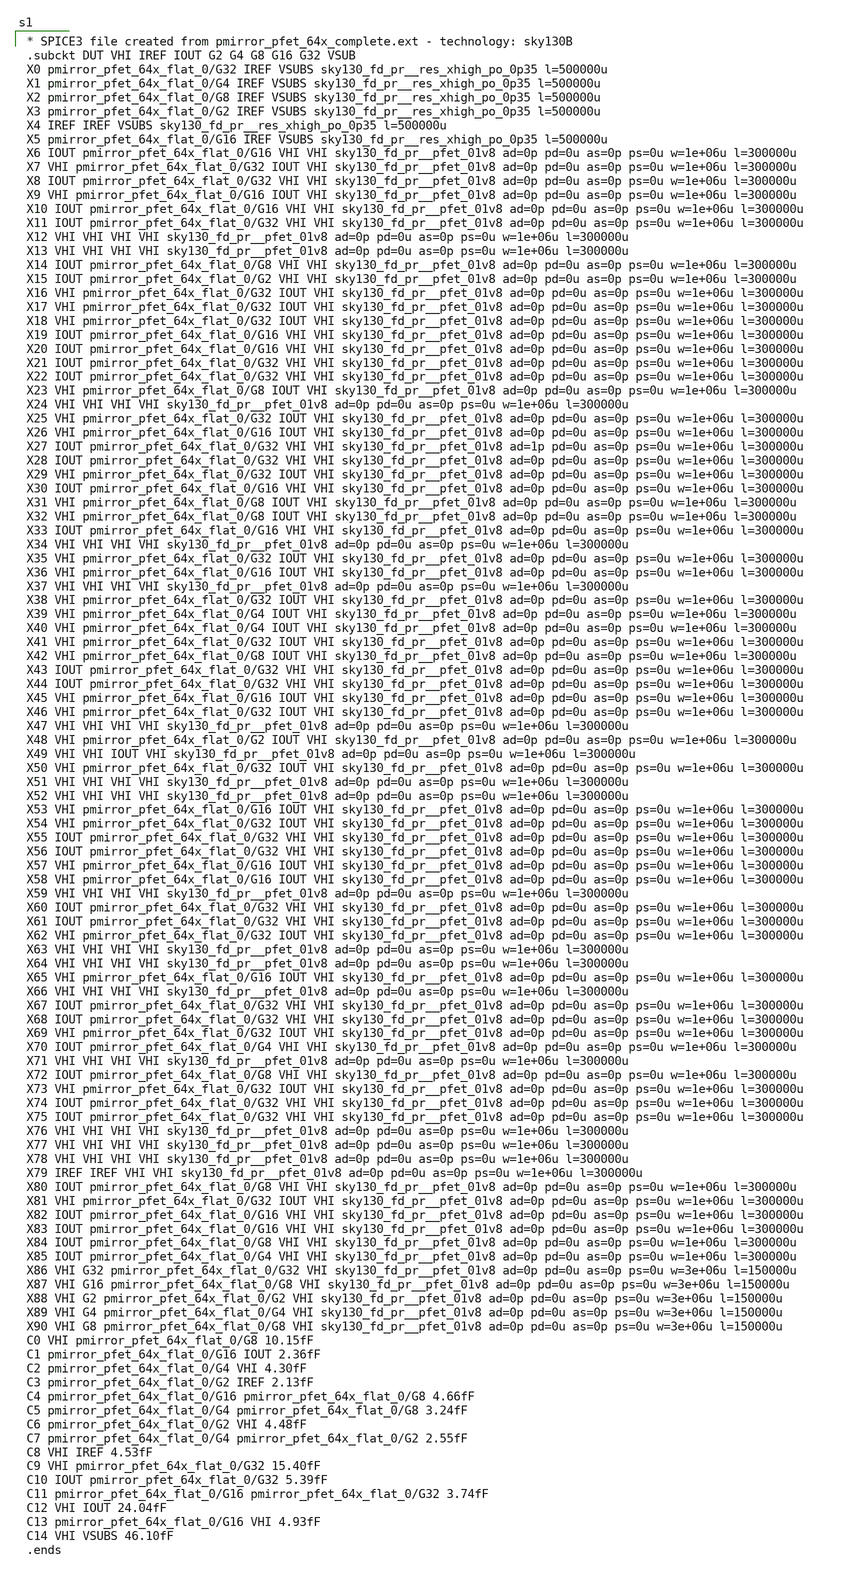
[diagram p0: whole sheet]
** sch_path: xschem/untitled-10.sch
**.subckt untitled-10
**** begin user architecture code

* SPICE3 file created from pmirror_pfet_64x_complete.ext - technology: sky130B
.subckt DUT VHI IREF IOUT G2 G4 G8 G16 G32 VSUB
X0 pmirror_pfet_64x_flat_0/G32 IREF VSUBS sky130_fd_pr__res_xhigh_po_0p35 l=500000u
X1 pmirror_pfet_64x_flat_0/G4 IREF VSUBS sky130_fd_pr__res_xhigh_po_0p35 l=500000u
X2 pmirror_pfet_64x_flat_0/G8 IREF VSUBS sky130_fd_pr__res_xhigh_po_0p35 l=500000u
X3 pmirror_pfet_64x_flat_0/G2 IREF VSUBS sky130_fd_pr__res_xhigh_po_0p35 l=500000u
X4 IREF IREF VSUBS sky130_fd_pr__res_xhigh_po_0p35 l=500000u
X5 pmirror_pfet_64x_flat_0/G16 IREF VSUBS sky130_fd_pr__res_xhigh_po_0p35 l=500000u
X6 IOUT pmirror_pfet_64x_flat_0/G16 VHI VHI sky130_fd_pr__pfet_01v8 ad=0p pd=0u as=0p ps=0u w=1e+06u
+ l=300000u
X7 VHI pmirror_pfet_64x_flat_0/G32 IOUT VHI sky130_fd_pr__pfet_01v8 ad=0p pd=0u as=0p ps=0u w=1e+06u
+ l=300000u
X8 IOUT pmirror_pfet_64x_flat_0/G32 VHI VHI sky130_fd_pr__pfet_01v8 ad=0p pd=0u as=0p ps=0u w=1e+06u
+ l=300000u
X9 VHI pmirror_pfet_64x_flat_0/G16 IOUT VHI sky130_fd_pr__pfet_01v8 ad=0p pd=0u as=0p ps=0u w=1e+06u
+ l=300000u
X10 IOUT pmirror_pfet_64x_flat_0/G16 VHI VHI sky130_fd_pr__pfet_01v8 ad=0p pd=0u as=0p ps=0u
+ w=1e+06u l=300000u
X11 IOUT pmirror_pfet_64x_flat_0/G32 VHI VHI sky130_fd_pr__pfet_01v8 ad=0p pd=0u as=0p ps=0u
+ w=1e+06u l=300000u
X12 VHI VHI VHI VHI sky130_fd_pr__pfet_01v8 ad=0p pd=0u as=0p ps=0u w=1e+06u l=300000u
X13 VHI VHI VHI VHI sky130_fd_pr__pfet_01v8 ad=0p pd=0u as=0p ps=0u w=1e+06u l=300000u
X14 IOUT pmirror_pfet_64x_flat_0/G8 VHI VHI sky130_fd_pr__pfet_01v8 ad=0p pd=0u as=0p ps=0u w=1e+06u
+ l=300000u
X15 IOUT pmirror_pfet_64x_flat_0/G2 VHI VHI sky130_fd_pr__pfet_01v8 ad=0p pd=0u as=0p ps=0u w=1e+06u
+ l=300000u
X16 VHI pmirror_pfet_64x_flat_0/G32 IOUT VHI sky130_fd_pr__pfet_01v8 ad=0p pd=0u as=0p ps=0u
+ w=1e+06u l=300000u
X17 VHI pmirror_pfet_64x_flat_0/G32 IOUT VHI sky130_fd_pr__pfet_01v8 ad=0p pd=0u as=0p ps=0u
+ w=1e+06u l=300000u
X18 VHI pmirror_pfet_64x_flat_0/G32 IOUT VHI sky130_fd_pr__pfet_01v8 ad=0p pd=0u as=0p ps=0u
+ w=1e+06u l=300000u
X19 IOUT pmirror_pfet_64x_flat_0/G16 VHI VHI sky130_fd_pr__pfet_01v8 ad=0p pd=0u as=0p ps=0u
+ w=1e+06u l=300000u
X20 IOUT pmirror_pfet_64x_flat_0/G16 VHI VHI sky130_fd_pr__pfet_01v8 ad=0p pd=0u as=0p ps=0u
+ w=1e+06u l=300000u
X21 IOUT pmirror_pfet_64x_flat_0/G32 VHI VHI sky130_fd_pr__pfet_01v8 ad=0p pd=0u as=0p ps=0u
+ w=1e+06u l=300000u
X22 IOUT pmirror_pfet_64x_flat_0/G32 VHI VHI sky130_fd_pr__pfet_01v8 ad=0p pd=0u as=0p ps=0u
+ w=1e+06u l=300000u
X23 VHI pmirror_pfet_64x_flat_0/G8 IOUT VHI sky130_fd_pr__pfet_01v8 ad=0p pd=0u as=0p ps=0u w=1e+06u
+ l=300000u
X24 VHI VHI VHI VHI sky130_fd_pr__pfet_01v8 ad=0p pd=0u as=0p ps=0u w=1e+06u l=300000u
X25 VHI pmirror_pfet_64x_flat_0/G32 IOUT VHI sky130_fd_pr__pfet_01v8 ad=0p pd=0u as=0p ps=0u
+ w=1e+06u l=300000u
X26 VHI pmirror_pfet_64x_flat_0/G16 IOUT VHI sky130_fd_pr__pfet_01v8 ad=0p pd=0u as=0p ps=0u
+ w=1e+06u l=300000u
X27 IOUT pmirror_pfet_64x_flat_0/G32 VHI VHI sky130_fd_pr__pfet_01v8 ad=1p pd=0u as=0p ps=0u
+ w=1e+06u l=300000u
X28 IOUT pmirror_pfet_64x_flat_0/G32 VHI VHI sky130_fd_pr__pfet_01v8 ad=0p pd=0u as=0p ps=0u
+ w=1e+06u l=300000u
X29 VHI pmirror_pfet_64x_flat_0/G32 IOUT VHI sky130_fd_pr__pfet_01v8 ad=0p pd=0u as=0p ps=0u
+ w=1e+06u l=300000u
X30 IOUT pmirror_pfet_64x_flat_0/G16 VHI VHI sky130_fd_pr__pfet_01v8 ad=0p pd=0u as=0p ps=0u
+ w=1e+06u l=300000u
X31 VHI pmirror_pfet_64x_flat_0/G8 IOUT VHI sky130_fd_pr__pfet_01v8 ad=0p pd=0u as=0p ps=0u w=1e+06u
+ l=300000u
X32 VHI pmirror_pfet_64x_flat_0/G8 IOUT VHI sky130_fd_pr__pfet_01v8 ad=0p pd=0u as=0p ps=0u w=1e+06u
+ l=300000u
X33 IOUT pmirror_pfet_64x_flat_0/G16 VHI VHI sky130_fd_pr__pfet_01v8 ad=0p pd=0u as=0p ps=0u
+ w=1e+06u l=300000u
X34 VHI VHI VHI VHI sky130_fd_pr__pfet_01v8 ad=0p pd=0u as=0p ps=0u w=1e+06u l=300000u
X35 VHI pmirror_pfet_64x_flat_0/G32 IOUT VHI sky130_fd_pr__pfet_01v8 ad=0p pd=0u as=0p ps=0u
+ w=1e+06u l=300000u
X36 VHI pmirror_pfet_64x_flat_0/G16 IOUT VHI sky130_fd_pr__pfet_01v8 ad=0p pd=0u as=0p ps=0u
+ w=1e+06u l=300000u
X37 VHI VHI VHI VHI sky130_fd_pr__pfet_01v8 ad=0p pd=0u as=0p ps=0u w=1e+06u l=300000u
X38 VHI pmirror_pfet_64x_flat_0/G32 IOUT VHI sky130_fd_pr__pfet_01v8 ad=0p pd=0u as=0p ps=0u
+ w=1e+06u l=300000u
X39 VHI pmirror_pfet_64x_flat_0/G4 IOUT VHI sky130_fd_pr__pfet_01v8 ad=0p pd=0u as=0p ps=0u w=1e+06u
+ l=300000u
X40 VHI pmirror_pfet_64x_flat_0/G4 IOUT VHI sky130_fd_pr__pfet_01v8 ad=0p pd=0u as=0p ps=0u w=1e+06u
+ l=300000u
X41 VHI pmirror_pfet_64x_flat_0/G32 IOUT VHI sky130_fd_pr__pfet_01v8 ad=0p pd=0u as=0p ps=0u
+ w=1e+06u l=300000u
X42 VHI pmirror_pfet_64x_flat_0/G8 IOUT VHI sky130_fd_pr__pfet_01v8 ad=0p pd=0u as=0p ps=0u w=1e+06u
+ l=300000u
X43 IOUT pmirror_pfet_64x_flat_0/G32 VHI VHI sky130_fd_pr__pfet_01v8 ad=0p pd=0u as=0p ps=0u
+ w=1e+06u l=300000u
X44 IOUT pmirror_pfet_64x_flat_0/G32 VHI VHI sky130_fd_pr__pfet_01v8 ad=0p pd=0u as=0p ps=0u
+ w=1e+06u l=300000u
X45 VHI pmirror_pfet_64x_flat_0/G16 IOUT VHI sky130_fd_pr__pfet_01v8 ad=0p pd=0u as=0p ps=0u
+ w=1e+06u l=300000u
X46 VHI pmirror_pfet_64x_flat_0/G32 IOUT VHI sky130_fd_pr__pfet_01v8 ad=0p pd=0u as=0p ps=0u
+ w=1e+06u l=300000u
X47 VHI VHI VHI VHI sky130_fd_pr__pfet_01v8 ad=0p pd=0u as=0p ps=0u w=1e+06u l=300000u
X48 VHI pmirror_pfet_64x_flat_0/G2 IOUT VHI sky130_fd_pr__pfet_01v8 ad=0p pd=0u as=0p ps=0u w=1e+06u
+ l=300000u
X49 VHI VHI IOUT VHI sky130_fd_pr__pfet_01v8 ad=0p pd=0u as=0p ps=0u w=1e+06u l=300000u
X50 VHI pmirror_pfet_64x_flat_0/G32 IOUT VHI sky130_fd_pr__pfet_01v8 ad=0p pd=0u as=0p ps=0u
+ w=1e+06u l=300000u
X51 VHI VHI VHI VHI sky130_fd_pr__pfet_01v8 ad=0p pd=0u as=0p ps=0u w=1e+06u l=300000u
X52 VHI VHI VHI VHI sky130_fd_pr__pfet_01v8 ad=0p pd=0u as=0p ps=0u w=1e+06u l=300000u
X53 VHI pmirror_pfet_64x_flat_0/G16 IOUT VHI sky130_fd_pr__pfet_01v8 ad=0p pd=0u as=0p ps=0u
+ w=1e+06u l=300000u
X54 VHI pmirror_pfet_64x_flat_0/G32 IOUT VHI sky130_fd_pr__pfet_01v8 ad=0p pd=0u as=0p ps=0u
+ w=1e+06u l=300000u
X55 IOUT pmirror_pfet_64x_flat_0/G32 VHI VHI sky130_fd_pr__pfet_01v8 ad=0p pd=0u as=0p ps=0u
+ w=1e+06u l=300000u
X56 IOUT pmirror_pfet_64x_flat_0/G32 VHI VHI sky130_fd_pr__pfet_01v8 ad=0p pd=0u as=0p ps=0u
+ w=1e+06u l=300000u
X57 VHI pmirror_pfet_64x_flat_0/G16 IOUT VHI sky130_fd_pr__pfet_01v8 ad=0p pd=0u as=0p ps=0u
+ w=1e+06u l=300000u
X58 VHI pmirror_pfet_64x_flat_0/G16 IOUT VHI sky130_fd_pr__pfet_01v8 ad=0p pd=0u as=0p ps=0u
+ w=1e+06u l=300000u
X59 VHI VHI VHI VHI sky130_fd_pr__pfet_01v8 ad=0p pd=0u as=0p ps=0u w=1e+06u l=300000u
X60 IOUT pmirror_pfet_64x_flat_0/G32 VHI VHI sky130_fd_pr__pfet_01v8 ad=0p pd=0u as=0p ps=0u
+ w=1e+06u l=300000u
X61 IOUT pmirror_pfet_64x_flat_0/G32 VHI VHI sky130_fd_pr__pfet_01v8 ad=0p pd=0u as=0p ps=0u
+ w=1e+06u l=300000u
X62 VHI pmirror_pfet_64x_flat_0/G32 IOUT VHI sky130_fd_pr__pfet_01v8 ad=0p pd=0u as=0p ps=0u
+ w=1e+06u l=300000u
X63 VHI VHI VHI VHI sky130_fd_pr__pfet_01v8 ad=0p pd=0u as=0p ps=0u w=1e+06u l=300000u
X64 VHI VHI VHI VHI sky130_fd_pr__pfet_01v8 ad=0p pd=0u as=0p ps=0u w=1e+06u l=300000u
X65 VHI pmirror_pfet_64x_flat_0/G16 IOUT VHI sky130_fd_pr__pfet_01v8 ad=0p pd=0u as=0p ps=0u
+ w=1e+06u l=300000u
X66 VHI VHI VHI VHI sky130_fd_pr__pfet_01v8 ad=0p pd=0u as=0p ps=0u w=1e+06u l=300000u
X67 IOUT pmirror_pfet_64x_flat_0/G32 VHI VHI sky130_fd_pr__pfet_01v8 ad=0p pd=0u as=0p ps=0u
+ w=1e+06u l=300000u
X68 IOUT pmirror_pfet_64x_flat_0/G32 VHI VHI sky130_fd_pr__pfet_01v8 ad=0p pd=0u as=0p ps=0u
+ w=1e+06u l=300000u
X69 VHI pmirror_pfet_64x_flat_0/G32 IOUT VHI sky130_fd_pr__pfet_01v8 ad=0p pd=0u as=0p ps=0u
+ w=1e+06u l=300000u
X70 IOUT pmirror_pfet_64x_flat_0/G4 VHI VHI sky130_fd_pr__pfet_01v8 ad=0p pd=0u as=0p ps=0u w=1e+06u
+ l=300000u
X71 VHI VHI VHI VHI sky130_fd_pr__pfet_01v8 ad=0p pd=0u as=0p ps=0u w=1e+06u l=300000u
X72 IOUT pmirror_pfet_64x_flat_0/G8 VHI VHI sky130_fd_pr__pfet_01v8 ad=0p pd=0u as=0p ps=0u w=1e+06u
+ l=300000u
X73 VHI pmirror_pfet_64x_flat_0/G32 IOUT VHI sky130_fd_pr__pfet_01v8 ad=0p pd=0u as=0p ps=0u
+ w=1e+06u l=300000u
X74 IOUT pmirror_pfet_64x_flat_0/G32 VHI VHI sky130_fd_pr__pfet_01v8 ad=0p pd=0u as=0p ps=0u
+ w=1e+06u l=300000u
X75 IOUT pmirror_pfet_64x_flat_0/G32 VHI VHI sky130_fd_pr__pfet_01v8 ad=0p pd=0u as=0p ps=0u
+ w=1e+06u l=300000u
X76 VHI VHI VHI VHI sky130_fd_pr__pfet_01v8 ad=0p pd=0u as=0p ps=0u w=1e+06u l=300000u
X77 VHI VHI VHI VHI sky130_fd_pr__pfet_01v8 ad=0p pd=0u as=0p ps=0u w=1e+06u l=300000u
X78 VHI VHI VHI VHI sky130_fd_pr__pfet_01v8 ad=0p pd=0u as=0p ps=0u w=1e+06u l=300000u
X79 IREF IREF VHI VHI sky130_fd_pr__pfet_01v8 ad=0p pd=0u as=0p ps=0u w=1e+06u l=300000u
X80 IOUT pmirror_pfet_64x_flat_0/G8 VHI VHI sky130_fd_pr__pfet_01v8 ad=0p pd=0u as=0p ps=0u w=1e+06u
+ l=300000u
X81 VHI pmirror_pfet_64x_flat_0/G32 IOUT VHI sky130_fd_pr__pfet_01v8 ad=0p pd=0u as=0p ps=0u
+ w=1e+06u l=300000u
X82 IOUT pmirror_pfet_64x_flat_0/G16 VHI VHI sky130_fd_pr__pfet_01v8 ad=0p pd=0u as=0p ps=0u
+ w=1e+06u l=300000u
X83 IOUT pmirror_pfet_64x_flat_0/G16 VHI VHI sky130_fd_pr__pfet_01v8 ad=0p pd=0u as=0p ps=0u
+ w=1e+06u l=300000u
X84 IOUT pmirror_pfet_64x_flat_0/G8 VHI VHI sky130_fd_pr__pfet_01v8 ad=0p pd=0u as=0p ps=0u w=1e+06u
+ l=300000u
X85 IOUT pmirror_pfet_64x_flat_0/G4 VHI VHI sky130_fd_pr__pfet_01v8 ad=0p pd=0u as=0p ps=0u w=1e+06u
+ l=300000u
X86 VHI G32 pmirror_pfet_64x_flat_0/G32 VHI sky130_fd_pr__pfet_01v8 ad=0p pd=0u as=0p ps=0u w=3e+06u
+ l=150000u
X87 VHI G16 pmirror_pfet_64x_flat_0/G8 VHI sky130_fd_pr__pfet_01v8 ad=0p pd=0u as=0p ps=0u w=3e+06u
+ l=150000u
X88 VHI G2 pmirror_pfet_64x_flat_0/G2 VHI sky130_fd_pr__pfet_01v8 ad=0p pd=0u as=0p ps=0u w=3e+06u
+ l=150000u
X89 VHI G4 pmirror_pfet_64x_flat_0/G4 VHI sky130_fd_pr__pfet_01v8 ad=0p pd=0u as=0p ps=0u w=3e+06u
+ l=150000u
X90 VHI G8 pmirror_pfet_64x_flat_0/G8 VHI sky130_fd_pr__pfet_01v8 ad=0p pd=0u as=0p ps=0u w=3e+06u
+ l=150000u
C0 VHI pmirror_pfet_64x_flat_0/G8 10.15fF
C1 pmirror_pfet_64x_flat_0/G16 IOUT 2.36fF
C2 pmirror_pfet_64x_flat_0/G4 VHI 4.30fF
C3 pmirror_pfet_64x_flat_0/G2 IREF 2.13fF
C4 pmirror_pfet_64x_flat_0/G16 pmirror_pfet_64x_flat_0/G8 4.66fF
C5 pmirror_pfet_64x_flat_0/G4 pmirror_pfet_64x_flat_0/G8 3.24fF
C6 pmirror_pfet_64x_flat_0/G2 VHI 4.48fF
C7 pmirror_pfet_64x_flat_0/G4 pmirror_pfet_64x_flat_0/G2 2.55fF
C8 VHI IREF 4.53fF
C9 VHI pmirror_pfet_64x_flat_0/G32 15.40fF
C10 IOUT pmirror_pfet_64x_flat_0/G32 5.39fF
C11 pmirror_pfet_64x_flat_0/G16 pmirror_pfet_64x_flat_0/G32 3.74fF
C12 VHI IOUT 24.04fF
C13 pmirror_pfet_64x_flat_0/G16 VHI 4.93fF
C14 VHI VSUBS 46.10fF
.ends



**** end user architecture code
**.ends
.end
